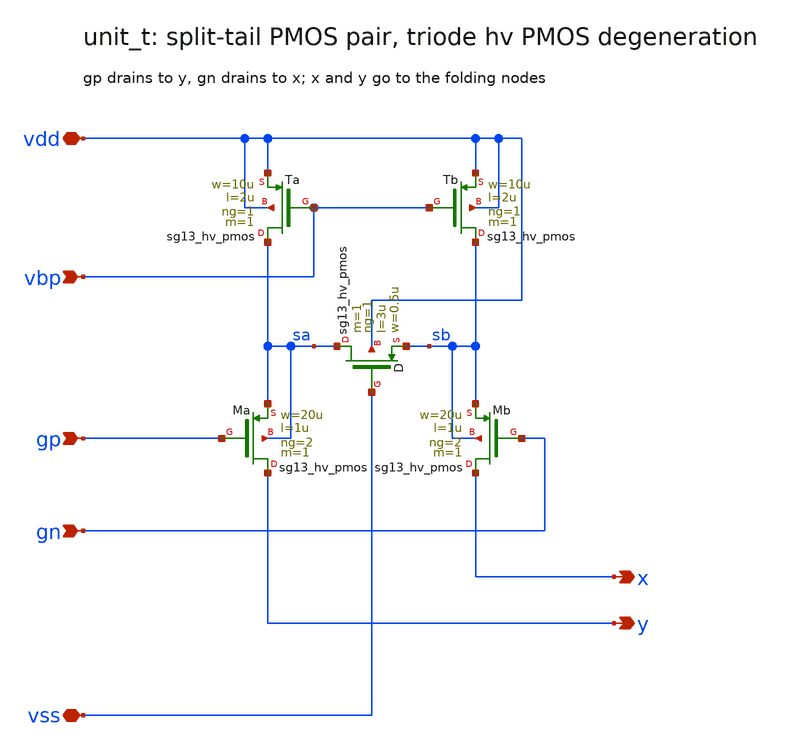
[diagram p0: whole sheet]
** sch_path: sudelbuecher/design_considerations/class_ab_pad_driver/improvements/xschem/unit_t.sch
**.subckt unit_t x y gp gn vdd vss vbp
*.opin x
*.opin y
*.ipin gp
*.ipin gn
*.iopin vdd
*.iopin vss
*.ipin vbp
XTa sa vbp vdd vdd sg13_hv_pmos w=10u l=2u ng=1 m=1 mm_ok=1
XTb sb vbp vdd vdd sg13_hv_pmos w=10u l=2u ng=1 m=1 mm_ok=1
XMa y gp sa sa sg13_hv_pmos w=20u l=1u ng=2 m=1 mm_ok=1
XMb x gn sb sb sg13_hv_pmos w=20u l=1u ng=2 m=1 mm_ok=1
XD sa vss sb vdd sg13_hv_pmos w=0.5u l=3u ng=1 m=1 mm_ok=1
**.ends
.end
